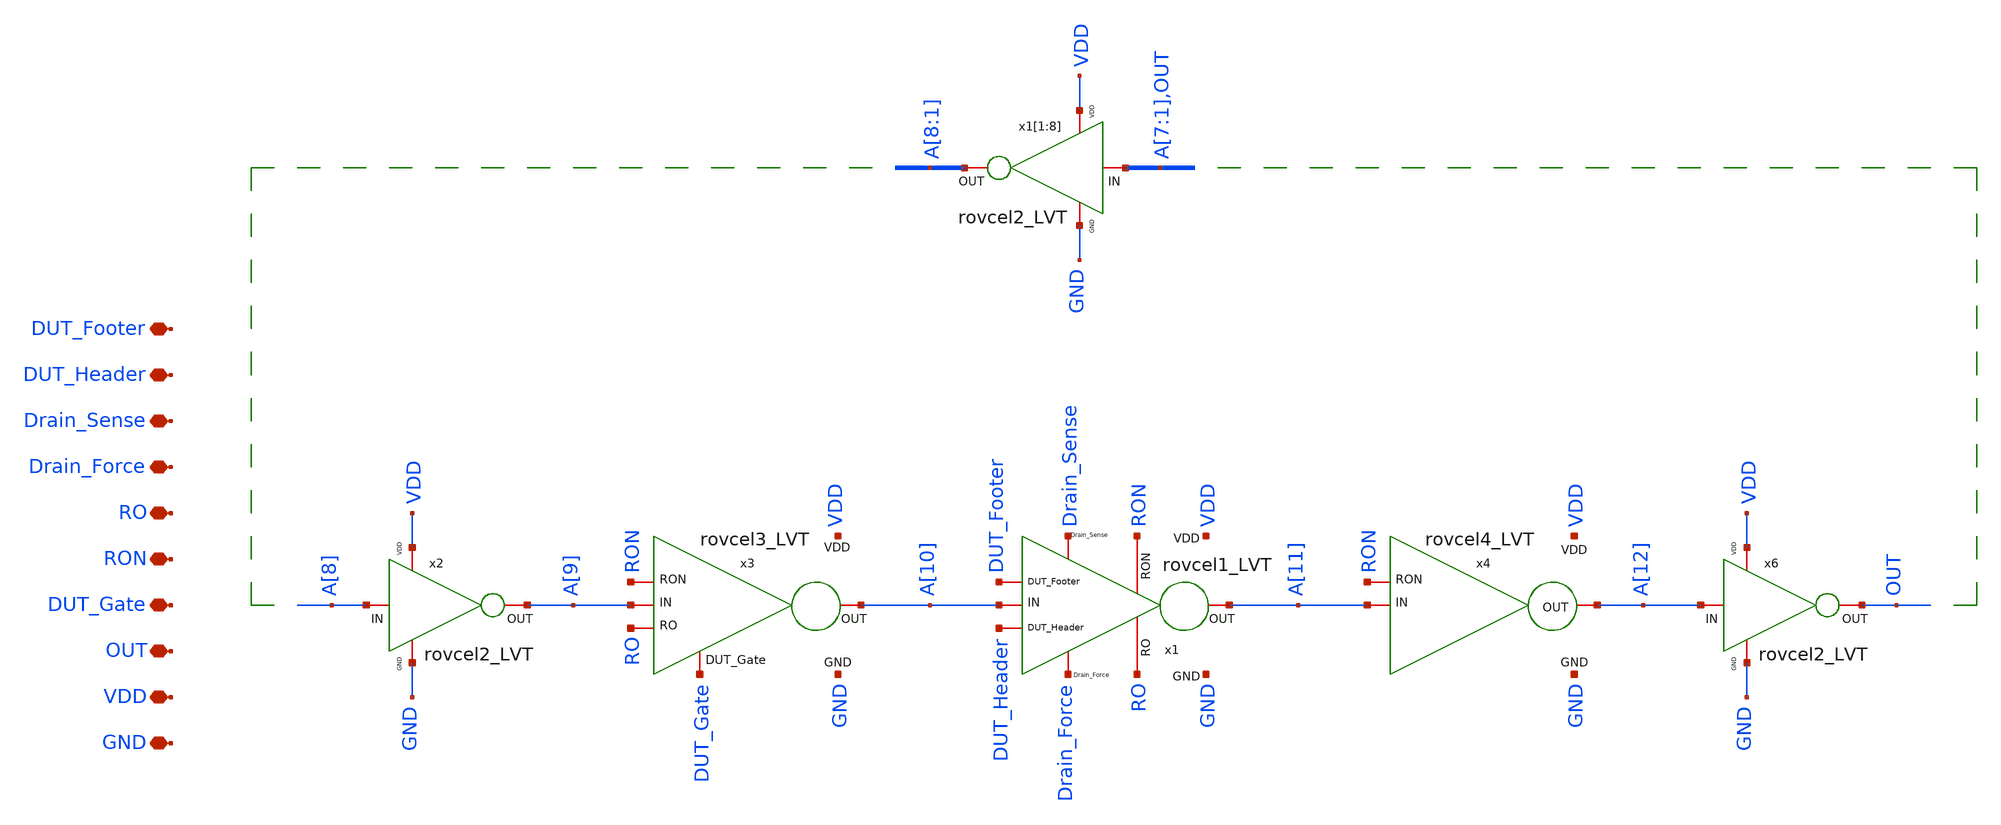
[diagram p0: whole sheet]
** sch_path: LVT/RO_LVT_13St/RO_LVT_13St.sch
**.subckt RO_LVT_13St DUT_Footer DUT_Header Drain_Sense Drain_Force RON RO DUT_Gate OUT GND VDD
*.iopin DUT_Footer
*.iopin DUT_Header
*.iopin Drain_Sense
*.iopin Drain_Force
*.iopin RON
*.iopin RO
*.iopin DUT_Gate
*.iopin OUT
*.iopin GND
*.iopin VDD
x1[1] VDD GND A[7] A[8] rovcel2_LVT
x1[2] VDD GND A[6] A[7] rovcel2_LVT
x1[3] VDD GND A[5] A[6] rovcel2_LVT
x1[4] VDD GND A[4] A[5] rovcel2_LVT
x1[5] VDD GND A[3] A[4] rovcel2_LVT
x1[6] VDD GND A[2] A[3] rovcel2_LVT
x1[7] VDD GND A[1] A[2] rovcel2_LVT
x1[8] VDD GND OUT A[1] rovcel2_LVT
x2 VDD GND A[8] A[9] rovcel2_LVT
x6 VDD GND A[12] OUT rovcel2_LVT
x1 VDD GND Drain_Sense DUT_Footer DUT_Header Drain_Force A[10] A[11] RON RO rovcel1_LVT
x3 VDD GND RON A[9] A[10] RO DUT_Gate rovcel3_LVT
x4 VDD A[12] GND RON A[11] rovcel4_LVT
**.ends
.end
